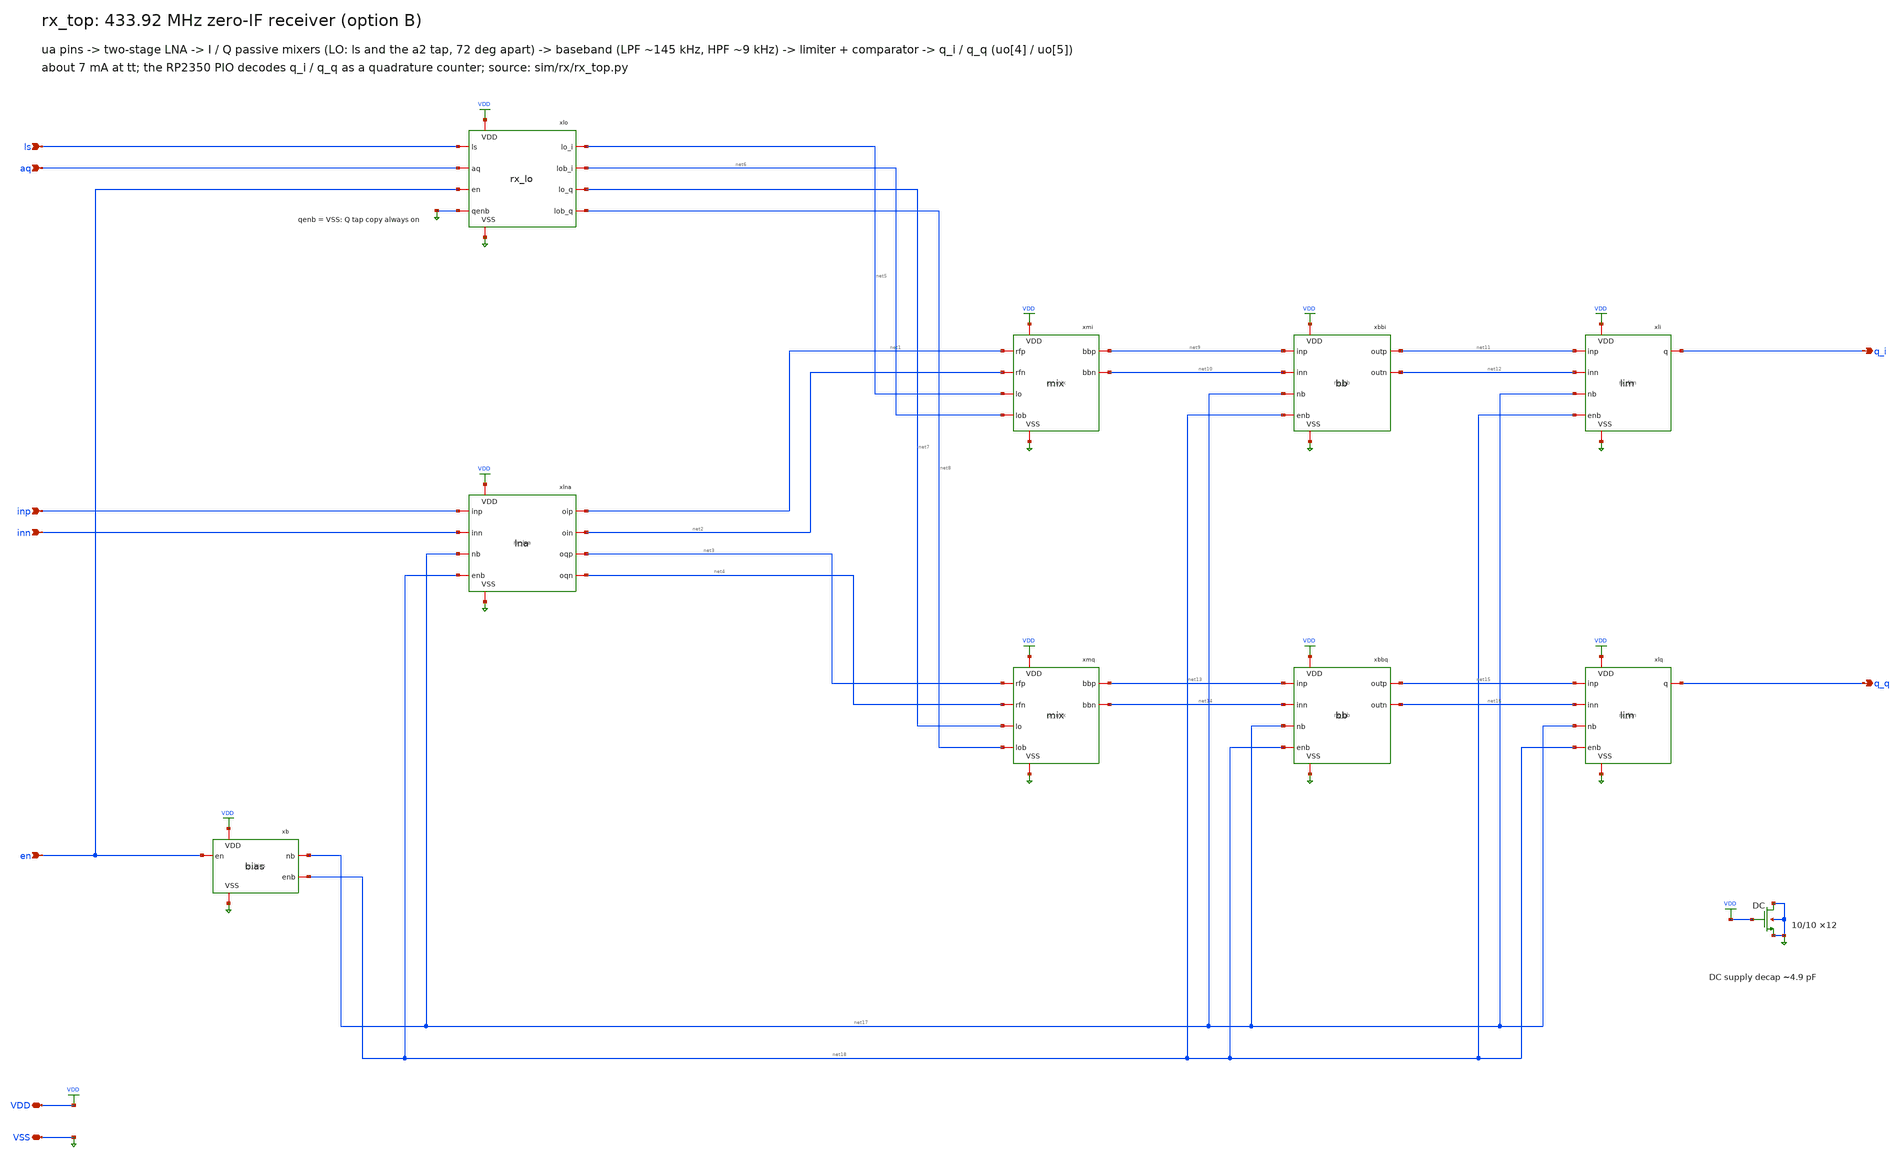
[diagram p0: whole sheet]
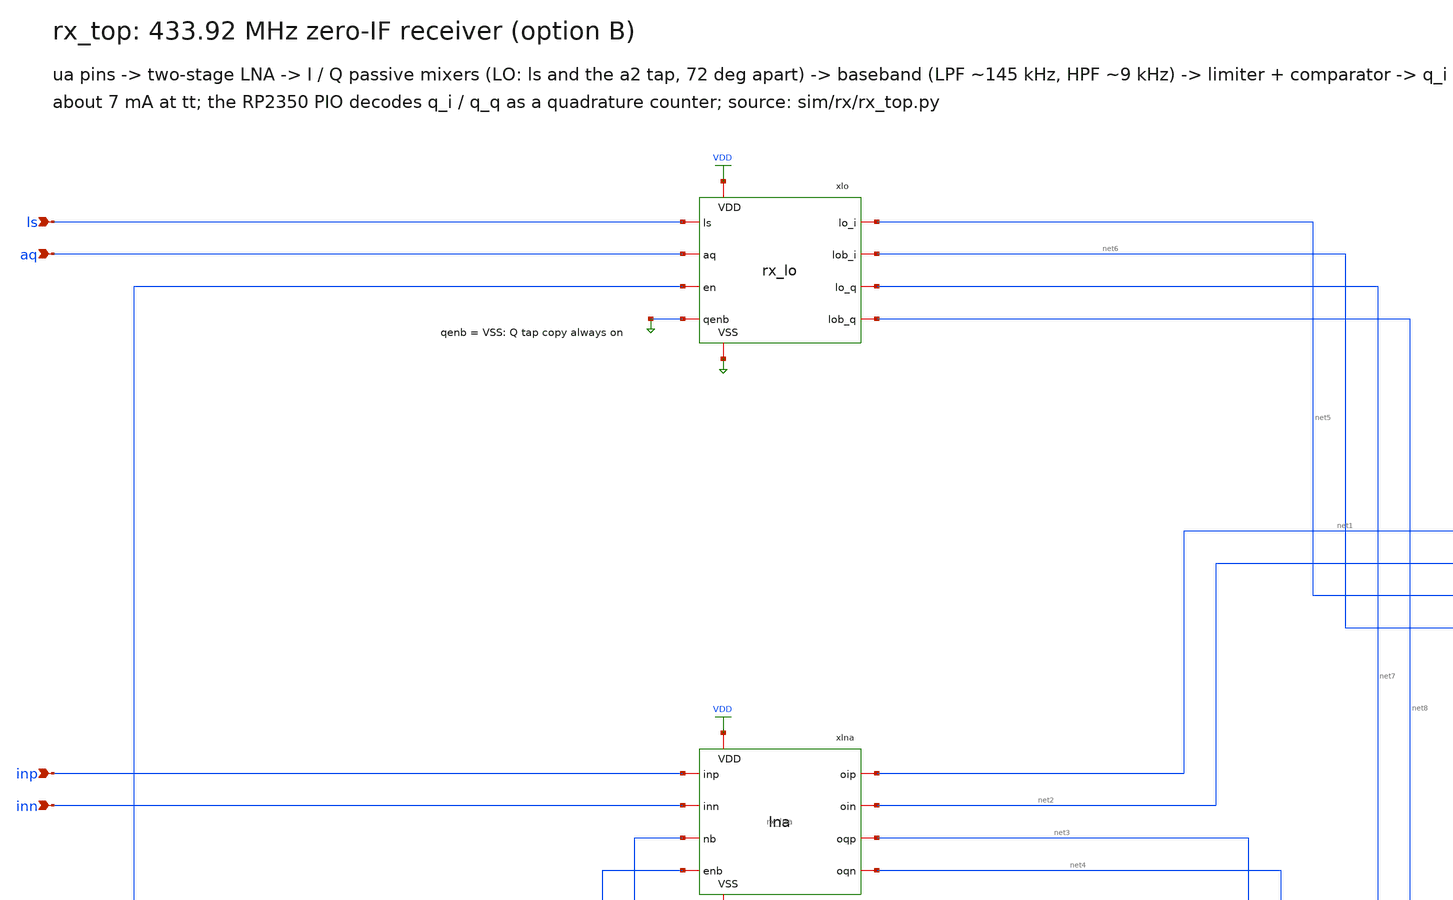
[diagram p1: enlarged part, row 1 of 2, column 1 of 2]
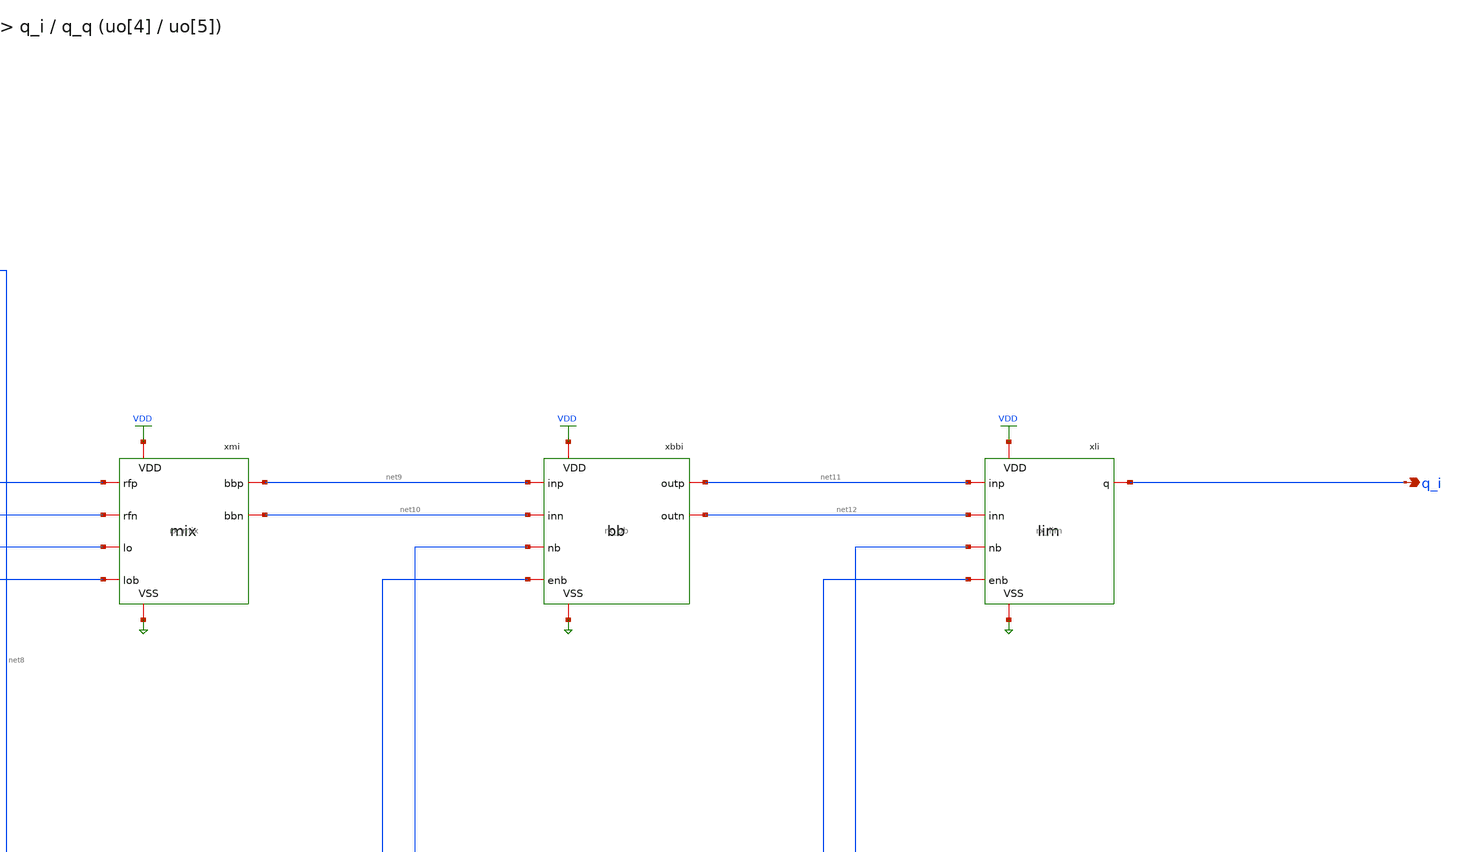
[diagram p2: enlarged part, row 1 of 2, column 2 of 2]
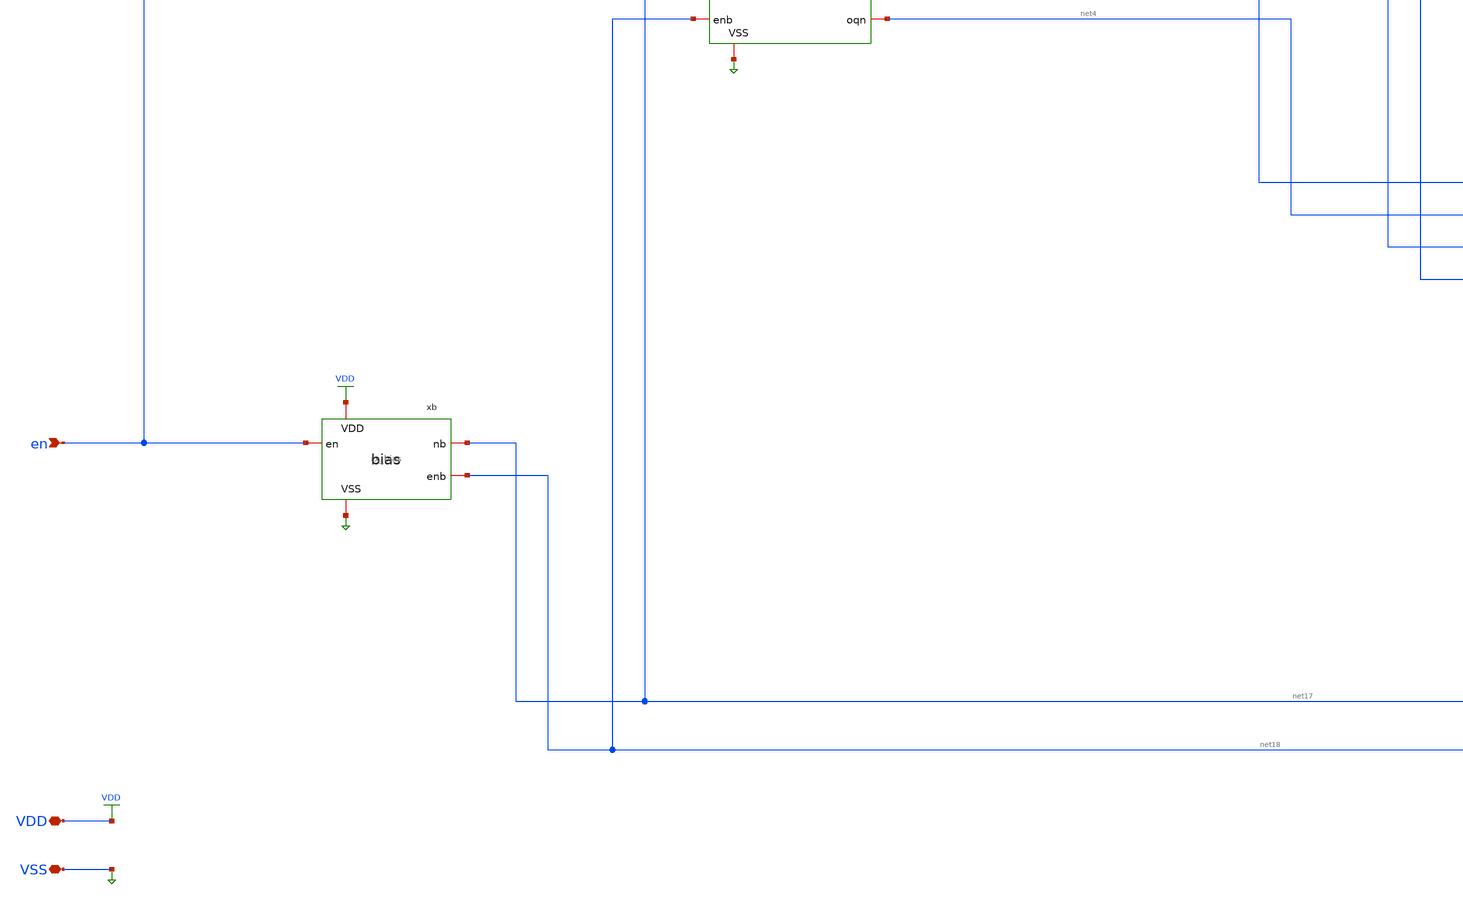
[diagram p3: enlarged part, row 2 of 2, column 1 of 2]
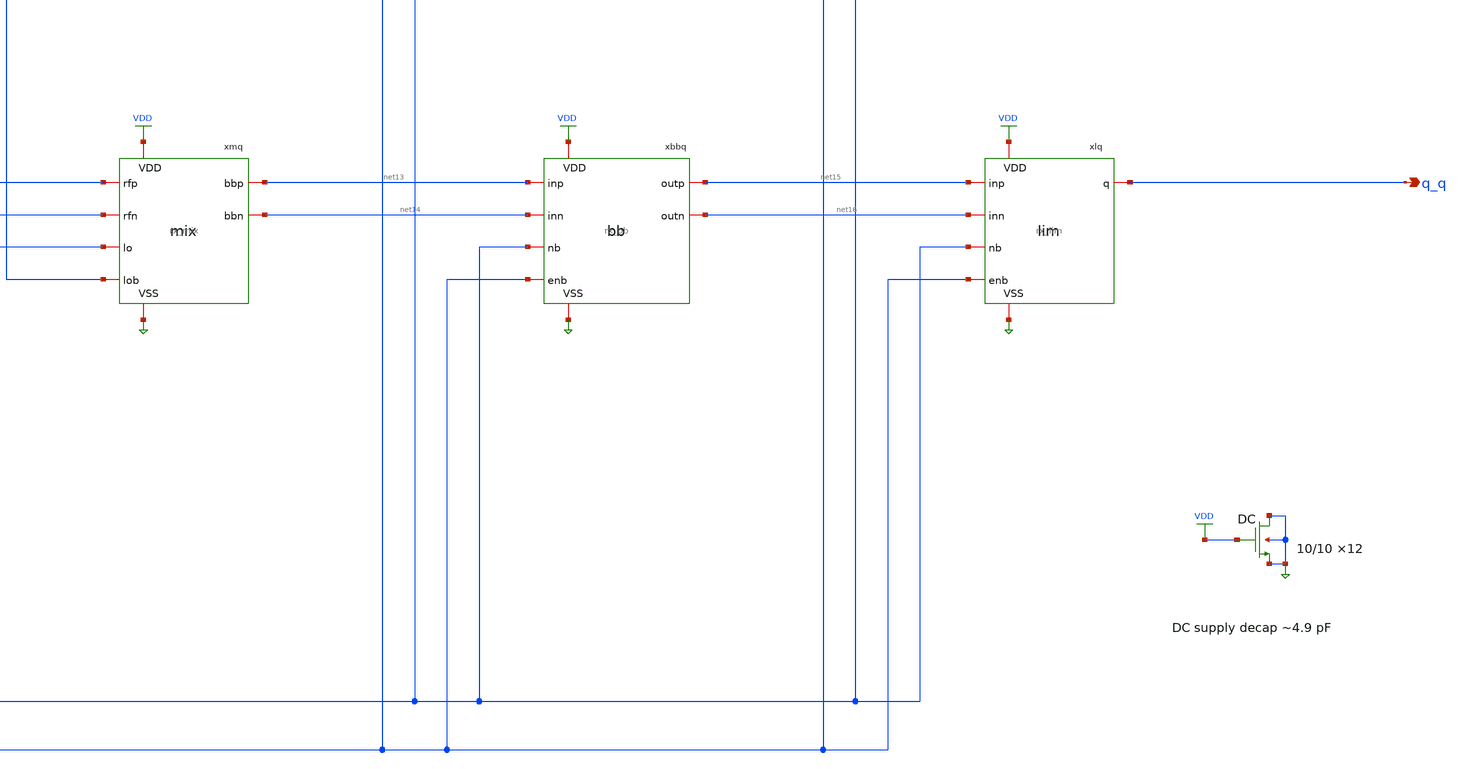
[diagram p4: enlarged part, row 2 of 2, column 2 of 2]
** sch_path: xschem/rx_top.sch
**.subckt rx_top VDD VSS inp inn ls aq en q_i q_q
*.iopin VDD
*.iopin VSS
*.ipin inp
*.ipin inn
*.ipin ls
*.ipin aq
*.ipin en
*.opin q_i
*.opin q_q
xb VDD VSS en net18 net17 rx_bias
xlna VDD VSS inp inn net1 net2 net3 net4 net17 net18 rx_lna
xlo VDD VSS ls aq en VSS net5 net6 net7 net8 rx_lo
xmi VDD VSS net1 net2 net9 net10 net5 net6 rx_mix
xmq VDD VSS net3 net4 net13 net14 net7 net8 rx_mix
xbbi VDD VSS net9 net10 net11 net12 net17 net18 rx_bb
xbbq VDD VSS net13 net14 net15 net16 net17 net18 rx_bb
xli VDD VSS net11 net12 q_i net17 net18 rx_lim
xlq VDD VSS net15 net16 q_q net17 net18 rx_lim
XDC VSS VDD VSS VSS nfet_03v3 L=10.0u W=10.0u nf=1 ad=5.0p as=5.0p pd=21.0u ps=21.0u nrd=0 nrs=0
+ sa=0 sb=0 sd=0 m=12
**.ends

* expanding   symbol:  rx_bias.sym # of pins=5
** sym_path: xschem/rx_bias.sym
** sch_path: xschem/rx_bias.sch
.subckt rx_bias VDD VSS en enb nb
*.iopin VDD
*.iopin VSS
*.ipin en
*.opin enb
*.opin nb
XMsw net2 enb VDD VDD pfet_03v3 L=0.28u W=4.0u nf=1 ad=2.0p as=2.0p pd=9.0u ps=9.0u nrd=0 nrs=0 sa=0
+ sb=0 sd=0 m=1
XMP1 nb net3 net2 VDD pfet_03v3 L=1.0u W=4.0u nf=1 ad=2.0p as=2.0p pd=9.0u ps=9.0u nrd=0 nrs=0 sa=0
+ sb=0 sd=0 m=2
XMP2 net3 net3 net2 VDD pfet_03v3 L=1.0u W=4.0u nf=1 ad=2.0p as=2.0p pd=9.0u ps=9.0u nrd=0 nrs=0
+ sa=0 sb=0 sd=0 m=2
XMN1 nb nb VSS VSS nfet_03v3 L=0.5u W=2.0u nf=1 ad=1.0p as=1.0p pd=5.0u ps=5.0u nrd=0 nrs=0 sa=0
+ sb=0 sd=0 m=1
XMN2 net3 nb net1 VSS nfet_03v3 L=0.5u W=2.0u nf=1 ad=1.0p as=1.0p pd=5.0u ps=5.0u nrd=0 nrs=0 sa=0
+ sb=0 sd=0 m=4
XMS1 net4 VSS net2 VDD pfet_03v3 L=10.0u W=0.41999999999999993u nf=1 ad=0.20999999999999996p
+ as=0.20999999999999996p pd=1.8399999999999999u ps=1.8399999999999999u nrd=0 nrs=0 sa=0 sb=0 sd=0 m=1
XMS2 net4 nb VSS VSS nfet_03v3 L=0.28u W=2.0u nf=1 ad=1.0p as=1.0p pd=5.0u ps=5.0u nrd=0 nrs=0 sa=0
+ sb=0 sd=0 m=1
XMS3 net3 net4 nb VSS nfet_03v3 L=0.28u W=1.0u nf=1 ad=0.5p as=0.5p pd=3.0u ps=3.0u nrd=0 nrs=0 sa=0
+ sb=0 sd=0 m=1
XMoff nb enb VSS VSS nfet_03v3 L=0.28u W=0.41999999999999993u nf=1 ad=0.20999999999999996p
+ as=0.20999999999999996p pd=1.8399999999999999u ps=1.8399999999999999u nrd=0 nrs=0 sa=0 sb=0 sd=0 m=1
XMoff2 net4 enb VSS VSS nfet_03v3 L=0.28u W=0.41999999999999993u nf=1 ad=0.20999999999999996p
+ as=0.20999999999999996p pd=1.8399999999999999u ps=1.8399999999999999u nrd=0 nrs=0 sa=0 sb=0 sd=0 m=1
XRb net1 VSS VSS ppolyf_u r_width=2.0e-6 r_length=29.714000000000002e-6 m=1
XCnb VSS nb VSS VSS nfet_03v3 L=10.0u W=24.57u nf=1 ad=12.285p as=12.285p pd=50.14u ps=50.14u nrd=0
+ nrs=0 sa=0 sb=0 sd=0 m=1
XIep enb en VDD VDD pfet_03v3 L=0.28u W=1.0u nf=1 ad=0.5p as=0.5p pd=3.0u ps=3.0u nrd=0 nrs=0 sa=0
+ sb=0 sd=0 m=1
XIen enb en VSS VSS nfet_03v3 L=0.28u W=0.41999999999999993u nf=1 ad=0.20999999999999996p
+ as=0.20999999999999996p pd=1.8399999999999999u ps=1.8399999999999999u nrd=0 nrs=0 sa=0 sb=0 sd=0 m=1
.ends


* expanding   symbol:  rx_lna.sym # of pins=10
** sym_path: xschem/rx_lna.sym
** sch_path: xschem/rx_lna.sch
.subckt rx_lna VDD VSS inp inn oip oin oqp oqn nb enb
*.iopin VDD
*.iopin VSS
*.ipin inp
*.ipin inn
*.opin oip
*.opin oin
*.opin oqp
*.opin oqn
*.ipin nb
*.ipin enb
XM1 net2 inp net1 VSS nfet_03v3 L=0.28u W=10.0u nf=1 ad=5.0p as=5.0p pd=21.0u ps=21.0u nrd=0 nrs=0
+ sa=0 sb=0 sd=0 m=24
XM2 net3 inn net1 VSS nfet_03v3 L=0.28u W=10.0u nf=1 ad=5.0p as=5.0p pd=21.0u ps=21.0u nrd=0 nrs=0
+ sa=0 sb=0 sd=0 m=24
XMt net1 nb VSS VSS nfet_03v3 L=0.5u W=2.0u nf=1 ad=1.0p as=1.0p pd=5.0u ps=5.0u nrd=0 nrs=0 sa=0
+ sb=0 sd=0 m=120
XRLp net2 VDD VSS ppolyf_u r_width=4.0e-6 r_length=9.143e-6 m=1
XRLn net3 VDD VSS ppolyf_u r_width=4.0e-6 r_length=9.143e-6 m=1
XRgp inp net4 VSS ppolyf_u_1k r_width=1.0e-6 r_length=20.0e-6 m=1
XRgn inn net4 VSS ppolyf_u_1k r_width=1.0e-6 r_length=20.0e-6 m=1
XMvs net5 enb VDD VDD pfet_03v3 L=0.28u W=2.0u nf=1 ad=1.0p as=1.0p pd=5.0u ps=5.0u nrd=0 nrs=0 sa=0
+ sb=0 sd=0 m=1
XRv1 net5 net4 VSS ppolyf_u_1k r_width=1.0e-6 r_length=40.0e-6 m=1
XRv2 net4 VSS VSS ppolyf_u_1k r_width=1.0e-6 r_length=30.0e-6 m=1
XCvcm VSS net4 VSS VSS nfet_03v3 L=10.0u W=49.14u nf=1 ad=24.57p as=24.57p pd=99.28u ps=99.28u nrd=0
+ nrs=0 sa=0 sb=0 sd=0 m=1
x2i VDD VSS net3 net2 oip oin nb rx_lna2
x2q VDD VSS net3 net2 oqp oqn nb rx_lna2
.ends


* expanding   symbol:  rx_lo.sym # of pins=10
** sym_path: xschem/rx_lo.sym
** sch_path: xschem/rx_lo.sch
.subckt rx_lo VDD VSS ls aq en qenb lo_i lob_i lo_q lob_q
*.iopin VDD
*.iopin VSS
*.ipin ls
*.ipin aq
*.ipin en
*.ipin qenb
*.opin lo_i
*.opin lob_i
*.opin lo_q
*.opin lob_q
xlq VDD VSS aq qenb net1 rx_lsq
xbi VDD VSS ls en lo_i lob_i rx_lobuf
xbq VDD VSS net1 en lo_q lob_q rx_lobuf
.ends


* expanding   symbol:  rx_mix.sym # of pins=8
** sym_path: xschem/rx_mix.sym
** sch_path: xschem/rx_mix.sch
.subckt rx_mix VDD VSS rfp rfn bbp bbn lo lob
*.iopin VDD
*.iopin VSS
*.ipin rfp
*.ipin rfn
*.opin bbp
*.opin bbn
*.ipin lo
*.ipin lob
XS1n bbp lo rfp VSS nfet_03v3 L=0.28u W=8.0u nf=1 ad=4.0p as=4.0p pd=17.0u ps=17.0u nrd=0 nrs=0 sa=0
+ sb=0 sd=0 m=1
XS1p bbp lob rfp VDD pfet_03v3 L=0.28u W=16.0u nf=1 ad=8.0p as=8.0p pd=33.0u ps=33.0u nrd=0 nrs=0
+ sa=0 sb=0 sd=0 m=1
XS4n bbn lob rfp VSS nfet_03v3 L=0.28u W=8.0u nf=1 ad=4.0p as=4.0p pd=17.0u ps=17.0u nrd=0 nrs=0
+ sa=0 sb=0 sd=0 m=1
XS4p bbn lo rfp VDD pfet_03v3 L=0.28u W=16.0u nf=1 ad=8.0p as=8.0p pd=33.0u ps=33.0u nrd=0 nrs=0
+ sa=0 sb=0 sd=0 m=1
XS3n bbp lob rfn VSS nfet_03v3 L=0.28u W=8.0u nf=1 ad=4.0p as=4.0p pd=17.0u ps=17.0u nrd=0 nrs=0
+ sa=0 sb=0 sd=0 m=1
XS3p bbp lo rfn VDD pfet_03v3 L=0.28u W=16.0u nf=1 ad=8.0p as=8.0p pd=33.0u ps=33.0u nrd=0 nrs=0
+ sa=0 sb=0 sd=0 m=1
XS2n bbn lo rfn VSS nfet_03v3 L=0.28u W=8.0u nf=1 ad=4.0p as=4.0p pd=17.0u ps=17.0u nrd=0 nrs=0 sa=0
+ sb=0 sd=0 m=1
XS2p bbn lob rfn VDD pfet_03v3 L=0.28u W=16.0u nf=1 ad=8.0p as=8.0p pd=33.0u ps=33.0u nrd=0 nrs=0
+ sa=0 sb=0 sd=0 m=1
XCbp VSS bbp VSS VSS nfet_03v3 L=5.0u W=24.57u nf=1 ad=12.285p as=12.285p pd=50.14u ps=50.14u nrd=0
+ nrs=0 sa=0 sb=0 sd=0 m=1
XCbn VSS bbn VSS VSS nfet_03v3 L=5.0u W=24.57u nf=1 ad=12.285p as=12.285p pd=50.14u ps=50.14u nrd=0
+ nrs=0 sa=0 sb=0 sd=0 m=1
.ends


* expanding   symbol:  rx_bb.sym # of pins=8
** sym_path: xschem/rx_bb.sym
** sch_path: xschem/rx_bb.sch
.subckt rx_bb VDD VSS inp inn outp outn nb enb
*.iopin VDD
*.iopin VSS
*.ipin inp
*.ipin inn
*.opin outp
*.opin outn
*.ipin nb
*.ipin enb
XMvbs net1 enb VDD VDD pfet_03v3 L=0.28u W=1.0u nf=1 ad=0.5p as=0.5p pd=3.0u ps=3.0u nrd=0 nrs=0
+ sa=0 sb=0 sd=0 m=1
XRvb1 net1 net2 VSS ppolyf_u_1k r_width=1.0e-6 r_length=150.0e-6 m=1
XRvb2 net2 VSS VSS ppolyf_u_1k r_width=1.0e-6 r_length=100.0e-6 m=1
XCvb VSS net2 VSS VSS nfet_03v3 L=10.0u W=24.57u nf=1 ad=12.285p as=12.285p pd=50.14u ps=50.14u
+ nrd=0 nrs=0 sa=0 sb=0 sd=0 m=1
XMvbrep net3 net3 net2 net2 pfet_03v3 L=1.0u W=4.0u nf=1 ad=2.0p as=2.0p pd=9.0u ps=9.0u nrd=0 nrs=0
+ sa=0 sb=0 sd=0 m=1
XMvbsnk net3 nb VSS VSS nfet_03v3 L=49.99999999999999u W=0.41999999999999993u nf=1
+ ad=0.20999999999999996p as=0.20999999999999996p pd=1.8399999999999999u ps=1.8399999999999999u nrd=0 nrs=0 sa=0 sb=0 sd=0
+ m=1
XM1a net5 inp net4 VSS nfet_03v3 L=1.0u W=20.0u nf=1 ad=10.0p as=10.0p pd=41.0u ps=41.0u nrd=0 nrs=0
+ sa=0 sb=0 sd=0 m=16
XM1b net6 inn net4 VSS nfet_03v3 L=1.0u W=20.0u nf=1 ad=10.0p as=10.0p pd=41.0u ps=41.0u nrd=0 nrs=0
+ sa=0 sb=0 sd=0 m=16
XMt1 net4 nb VSS VSS nfet_03v3 L=0.5u W=2.0u nf=1 ad=1.0p as=1.0p pd=5.0u ps=5.0u nrd=0 nrs=0 sa=0
+ sb=0 sd=0 m=8
XR1a net5 VDD VSS ppolyf_u r_width=2.0e-6 r_length=57.143e-6 m=1
XR1b net6 VDD VSS ppolyf_u r_width=2.0e-6 r_length=57.143e-6 m=1
XCc2a net6 net7 net6 net6 pfet_03v3 L=10.0u W=24.57u nf=1 ad=12.285p as=12.285p pd=50.14u ps=50.14u
+ nrd=0 nrs=0 sa=0 sb=0 sd=0 m=1
XRp2ar net7 net3 net2 net2 pfet_03v3 L=12.0u W=0.41999999999999993u nf=1 ad=0.20999999999999996p
+ as=0.20999999999999996p pd=1.8399999999999999u ps=1.8399999999999999u nrd=0 nrs=0 sa=0 sb=0 sd=0 m=1
XRp2aa net8 net8 net7 net7 pfet_03v3 L=1.0u W=0.41999999999999993u nf=1 ad=0.20999999999999996p
+ as=0.20999999999999996p pd=1.8399999999999999u ps=1.8399999999999999u nrd=0 nrs=0 sa=0 sb=0 sd=0 m=1
XRp2ab net8 net8 net2 net2 pfet_03v3 L=1.0u W=0.41999999999999993u nf=1 ad=0.20999999999999996p
+ as=0.20999999999999996p pd=1.8399999999999999u ps=1.8399999999999999u nrd=0 nrs=0 sa=0 sb=0 sd=0 m=1
XCc2b net5 net9 net5 net5 pfet_03v3 L=10.0u W=24.57u nf=1 ad=12.285p as=12.285p pd=50.14u ps=50.14u
+ nrd=0 nrs=0 sa=0 sb=0 sd=0 m=1
XRp2br net9 net3 net2 net2 pfet_03v3 L=12.0u W=0.41999999999999993u nf=1 ad=0.20999999999999996p
+ as=0.20999999999999996p pd=1.8399999999999999u ps=1.8399999999999999u nrd=0 nrs=0 sa=0 sb=0 sd=0 m=1
XRp2ba net10 net10 net9 net9 pfet_03v3 L=1.0u W=0.41999999999999993u nf=1 ad=0.20999999999999996p
+ as=0.20999999999999996p pd=1.8399999999999999u ps=1.8399999999999999u nrd=0 nrs=0 sa=0 sb=0 sd=0 m=1
XRp2bb net10 net10 net2 net2 pfet_03v3 L=1.0u W=0.41999999999999993u nf=1 ad=0.20999999999999996p
+ as=0.20999999999999996p pd=1.8399999999999999u ps=1.8399999999999999u nrd=0 nrs=0 sa=0 sb=0 sd=0 m=1
XM2a net12 net7 net11 VSS nfet_03v3 L=1.0u W=4.0u nf=1 ad=2.0p as=2.0p pd=9.0u ps=9.0u nrd=0 nrs=0
+ sa=0 sb=0 sd=0 m=2
XM2b net13 net9 net11 VSS nfet_03v3 L=1.0u W=4.0u nf=1 ad=2.0p as=2.0p pd=9.0u ps=9.0u nrd=0 nrs=0
+ sa=0 sb=0 sd=0 m=2
XMt2f net11 nb VSS VSS nfet_03v3 L=0.5u W=0.3u nf=1 ad=0.15p as=0.15p pd=1.6u ps=1.6u nrd=0 nrs=0
+ sa=0 sb=0 sd=0 m=1
XR2a net12 VDD VSS ppolyf_u_1k r_width=1.0e-6 r_length=200.0e-6 m=1
XR2b net13 VDD VSS ppolyf_u_1k r_width=1.0e-6 r_length=200.0e-6 m=1
XC2a VSS net12 VSS VSS nfet_03v3 L=10.0u W=98.28009999999999u nf=1 ad=49.140049999999995p
+ as=49.140049999999995p pd=197.56019999999998u ps=197.56019999999998u nrd=0 nrs=0 sa=0 sb=0 sd=0 m=1
XC2b VSS net13 VSS VSS nfet_03v3 L=10.0u W=98.28009999999999u nf=1 ad=49.140049999999995p
+ as=49.140049999999995p pd=197.56019999999998u ps=197.56019999999998u nrd=0 nrs=0 sa=0 sb=0 sd=0 m=1
XCc3a net13 net14 net13 net13 pfet_03v3 L=10.0u W=24.57u nf=1 ad=12.285p as=12.285p pd=50.14u
+ ps=50.14u nrd=0 nrs=0 sa=0 sb=0 sd=0 m=1
XRp3ar net14 net3 net2 net2 pfet_03v3 L=12.0u W=0.41999999999999993u nf=1 ad=0.20999999999999996p
+ as=0.20999999999999996p pd=1.8399999999999999u ps=1.8399999999999999u nrd=0 nrs=0 sa=0 sb=0 sd=0 m=1
XRp3aa net15 net15 net14 net14 pfet_03v3 L=1.0u W=0.41999999999999993u nf=1 ad=0.20999999999999996p
+ as=0.20999999999999996p pd=1.8399999999999999u ps=1.8399999999999999u nrd=0 nrs=0 sa=0 sb=0 sd=0 m=1
XRp3ab net15 net15 net2 net2 pfet_03v3 L=1.0u W=0.41999999999999993u nf=1 ad=0.20999999999999996p
+ as=0.20999999999999996p pd=1.8399999999999999u ps=1.8399999999999999u nrd=0 nrs=0 sa=0 sb=0 sd=0 m=1
XCc3b net12 net16 net12 net12 pfet_03v3 L=10.0u W=24.57u nf=1 ad=12.285p as=12.285p pd=50.14u
+ ps=50.14u nrd=0 nrs=0 sa=0 sb=0 sd=0 m=1
XRp3br net16 net3 net2 net2 pfet_03v3 L=12.0u W=0.41999999999999993u nf=1 ad=0.20999999999999996p
+ as=0.20999999999999996p pd=1.8399999999999999u ps=1.8399999999999999u nrd=0 nrs=0 sa=0 sb=0 sd=0 m=1
XRp3ba net17 net17 net16 net16 pfet_03v3 L=1.0u W=0.41999999999999993u nf=1 ad=0.20999999999999996p
+ as=0.20999999999999996p pd=1.8399999999999999u ps=1.8399999999999999u nrd=0 nrs=0 sa=0 sb=0 sd=0 m=1
XRp3bb net17 net17 net2 net2 pfet_03v3 L=1.0u W=0.41999999999999993u nf=1 ad=0.20999999999999996p
+ as=0.20999999999999996p pd=1.8399999999999999u ps=1.8399999999999999u nrd=0 nrs=0 sa=0 sb=0 sd=0 m=1
XM3a outn net14 net18 VSS nfet_03v3 L=1.0u W=4.0u nf=1 ad=2.0p as=2.0p pd=9.0u ps=9.0u nrd=0 nrs=0
+ sa=0 sb=0 sd=0 m=2
XM3b outp net16 net18 VSS nfet_03v3 L=1.0u W=4.0u nf=1 ad=2.0p as=2.0p pd=9.0u ps=9.0u nrd=0 nrs=0
+ sa=0 sb=0 sd=0 m=2
XMt3f net18 nb VSS VSS nfet_03v3 L=0.5u W=0.7999999999999999u nf=1 ad=0.39999999999999997p
+ as=0.39999999999999997p pd=2.5999999999999996u ps=2.5999999999999996u nrd=0 nrs=0 sa=0 sb=0 sd=0 m=1
XR3a outn VDD VSS ppolyf_u_1k r_width=1.0e-6 r_length=200.0e-6 m=1
XR3b outp VDD VSS ppolyf_u_1k r_width=1.0e-6 r_length=200.0e-6 m=1
XC3a VSS outn VSS VSS nfet_03v3 L=10.0u W=98.28009999999999u nf=1 ad=49.140049999999995p
+ as=49.140049999999995p pd=197.56019999999998u ps=197.56019999999998u nrd=0 nrs=0 sa=0 sb=0 sd=0 m=1
XC3b VSS outp VSS VSS nfet_03v3 L=10.0u W=98.28009999999999u nf=1 ad=49.140049999999995p
+ as=49.140049999999995p pd=197.56019999999998u ps=197.56019999999998u nrd=0 nrs=0 sa=0 sb=0 sd=0 m=1
.ends


* expanding   symbol:  rx_lim.sym # of pins=7
** sym_path: xschem/rx_lim.sym
** sch_path: xschem/rx_lim.sch
.subckt rx_lim VDD VSS inp inn q nb enb
*.iopin VDD
*.iopin VSS
*.ipin inp
*.ipin inn
*.opin q
*.ipin nb
*.ipin enb
XMvbs net1 enb VDD VDD pfet_03v3 L=0.28u W=1.0u nf=1 ad=0.5p as=0.5p pd=3.0u ps=3.0u nrd=0 nrs=0
+ sa=0 sb=0 sd=0 m=1
XRvb1 net1 net2 VSS ppolyf_u_1k r_width=1.0e-6 r_length=150.0e-6 m=1
XRvb2 net2 VSS VSS ppolyf_u_1k r_width=1.0e-6 r_length=100.0e-6 m=1
XCvb VSS net2 VSS VSS nfet_03v3 L=10.0u W=24.57u nf=1 ad=12.285p as=12.285p pd=50.14u ps=50.14u
+ nrd=0 nrs=0 sa=0 sb=0 sd=0 m=1
XMvbrep net3 net3 net2 net2 pfet_03v3 L=1.0u W=4.0u nf=1 ad=2.0p as=2.0p pd=9.0u ps=9.0u nrd=0 nrs=0
+ sa=0 sb=0 sd=0 m=1
XMvbsnk net3 nb VSS VSS nfet_03v3 L=49.99999999999999u W=0.41999999999999993u nf=1
+ ad=0.20999999999999996p as=0.20999999999999996p pd=1.8399999999999999u ps=1.8399999999999999u nrd=0 nrs=0 sa=0 sb=0 sd=0
+ m=1
XCcLa inp net4 inp inp pfet_03v3 L=10.0u W=12.285u nf=1 ad=6.1425p as=6.1425p pd=25.57u ps=25.57u
+ nrd=0 nrs=0 sa=0 sb=0 sd=0 m=1
XRpLar net4 net3 net2 net2 pfet_03v3 L=12.0u W=0.41999999999999993u nf=1 ad=0.20999999999999996p
+ as=0.20999999999999996p pd=1.8399999999999999u ps=1.8399999999999999u nrd=0 nrs=0 sa=0 sb=0 sd=0 m=1
XRpLaa net5 net5 net4 net4 pfet_03v3 L=1.0u W=0.41999999999999993u nf=1 ad=0.20999999999999996p
+ as=0.20999999999999996p pd=1.8399999999999999u ps=1.8399999999999999u nrd=0 nrs=0 sa=0 sb=0 sd=0 m=1
XRpLab net5 net5 net2 net2 pfet_03v3 L=1.0u W=0.41999999999999993u nf=1 ad=0.20999999999999996p
+ as=0.20999999999999996p pd=1.8399999999999999u ps=1.8399999999999999u nrd=0 nrs=0 sa=0 sb=0 sd=0 m=1
XCcLb inn net6 inn inn pfet_03v3 L=10.0u W=12.285u nf=1 ad=6.1425p as=6.1425p pd=25.57u ps=25.57u
+ nrd=0 nrs=0 sa=0 sb=0 sd=0 m=1
XRpLbr net6 net3 net2 net2 pfet_03v3 L=12.0u W=0.41999999999999993u nf=1 ad=0.20999999999999996p
+ as=0.20999999999999996p pd=1.8399999999999999u ps=1.8399999999999999u nrd=0 nrs=0 sa=0 sb=0 sd=0 m=1
XRpLba net7 net7 net6 net6 pfet_03v3 L=1.0u W=0.41999999999999993u nf=1 ad=0.20999999999999996p
+ as=0.20999999999999996p pd=1.8399999999999999u ps=1.8399999999999999u nrd=0 nrs=0 sa=0 sb=0 sd=0 m=1
XRpLbb net7 net7 net2 net2 pfet_03v3 L=1.0u W=0.41999999999999993u nf=1 ad=0.20999999999999996p
+ as=0.20999999999999996p pd=1.8399999999999999u ps=1.8399999999999999u nrd=0 nrs=0 sa=0 sb=0 sd=0 m=1
XMLa net9 net4 net8 VSS nfet_03v3 L=0.5u W=4.0u nf=1 ad=2.0p as=2.0p pd=9.0u ps=9.0u nrd=0 nrs=0
+ sa=0 sb=0 sd=0 m=2
XMLb net10 net6 net8 VSS nfet_03v3 L=0.5u W=4.0u nf=1 ad=2.0p as=2.0p pd=9.0u ps=9.0u nrd=0 nrs=0
+ sa=0 sb=0 sd=0 m=2
XMtL net8 nb VSS VSS nfet_03v3 L=0.5u W=2.0u nf=1 ad=1.0p as=1.0p pd=5.0u ps=5.0u nrd=0 nrs=0 sa=0
+ sb=0 sd=0 m=1
XRLa net9 VDD VSS ppolyf_u r_width=1.0e-6 r_length=28.571e-6 m=1
XRLb net10 VDD VSS ppolyf_u r_width=1.0e-6 r_length=28.571e-6 m=1
XCcCa net10 net11 net10 net10 pfet_03v3 L=10.0u W=12.285u nf=1 ad=6.1425p as=6.1425p pd=25.57u
+ ps=25.57u nrd=0 nrs=0 sa=0 sb=0 sd=0 m=1
XRpCar net11 net3 net2 net2 pfet_03v3 L=12.0u W=0.41999999999999993u nf=1 ad=0.20999999999999996p
+ as=0.20999999999999996p pd=1.8399999999999999u ps=1.8399999999999999u nrd=0 nrs=0 sa=0 sb=0 sd=0 m=1
XRpCaa net12 net12 net11 net11 pfet_03v3 L=1.0u W=0.41999999999999993u nf=1 ad=0.20999999999999996p
+ as=0.20999999999999996p pd=1.8399999999999999u ps=1.8399999999999999u nrd=0 nrs=0 sa=0 sb=0 sd=0 m=1
XRpCab net12 net12 net2 net2 pfet_03v3 L=1.0u W=0.41999999999999993u nf=1 ad=0.20999999999999996p
+ as=0.20999999999999996p pd=1.8399999999999999u ps=1.8399999999999999u nrd=0 nrs=0 sa=0 sb=0 sd=0 m=1
XCcCb net9 net13 net9 net9 pfet_03v3 L=10.0u W=12.285u nf=1 ad=6.1425p as=6.1425p pd=25.57u
+ ps=25.57u nrd=0 nrs=0 sa=0 sb=0 sd=0 m=1
XRpCbr net13 net3 net2 net2 pfet_03v3 L=12.0u W=0.41999999999999993u nf=1 ad=0.20999999999999996p
+ as=0.20999999999999996p pd=1.8399999999999999u ps=1.8399999999999999u nrd=0 nrs=0 sa=0 sb=0 sd=0 m=1
XRpCba net14 net14 net13 net13 pfet_03v3 L=1.0u W=0.41999999999999993u nf=1 ad=0.20999999999999996p
+ as=0.20999999999999996p pd=1.8399999999999999u ps=1.8399999999999999u nrd=0 nrs=0 sa=0 sb=0 sd=0 m=1
XRpCbb net14 net14 net2 net2 pfet_03v3 L=1.0u W=0.41999999999999993u nf=1 ad=0.20999999999999996p
+ as=0.20999999999999996p pd=1.8399999999999999u ps=1.8399999999999999u nrd=0 nrs=0 sa=0 sb=0 sd=0 m=1
XC1 net16 net11 net15 VSS nfet_03v3 L=0.5u W=2.0u nf=1 ad=1.0p as=1.0p pd=5.0u ps=5.0u nrd=0 nrs=0
+ sa=0 sb=0 sd=0 m=2
XC2 net17 net13 net15 VSS nfet_03v3 L=0.5u W=2.0u nf=1 ad=1.0p as=1.0p pd=5.0u ps=5.0u nrd=0 nrs=0
+ sa=0 sb=0 sd=0 m=2
XCt net15 nb VSS VSS nfet_03v3 L=0.5u W=2.0u nf=1 ad=1.0p as=1.0p pd=5.0u ps=5.0u nrd=0 nrs=0 sa=0
+ sb=0 sd=0 m=1
XC3 net16 net16 VDD VDD pfet_03v3 L=0.5u W=1.0u nf=1 ad=0.5p as=0.5p pd=3.0u ps=3.0u nrd=0 nrs=0
+ sa=0 sb=0 sd=0 m=1
XC5 net16 net17 VDD VDD pfet_03v3 L=0.5u W=1.6999999999999997u nf=1 ad=0.8499999999999999p
+ as=0.8499999999999999p pd=4.3999999999999995u ps=4.3999999999999995u nrd=0 nrs=0 sa=0 sb=0 sd=0 m=1
XC4 net17 net17 VDD VDD pfet_03v3 L=0.5u W=1.0u nf=1 ad=0.5p as=0.5p pd=3.0u ps=3.0u nrd=0 nrs=0
+ sa=0 sb=0 sd=0 m=1
XC6 net17 net16 VDD VDD pfet_03v3 L=0.5u W=1.6999999999999997u nf=1 ad=0.8499999999999999p
+ as=0.8499999999999999p pd=4.3999999999999995u ps=4.3999999999999995u nrd=0 nrs=0 sa=0 sb=0 sd=0 m=1
XC7 net18 net17 VDD VDD pfet_03v3 L=0.5u W=2.0u nf=1 ad=1.0p as=1.0p pd=5.0u ps=5.0u nrd=0 nrs=0
+ sa=0 sb=0 sd=0 m=1
XC8 net19 net16 VDD VDD pfet_03v3 L=0.5u W=2.0u nf=1 ad=1.0p as=1.0p pd=5.0u ps=5.0u nrd=0 nrs=0
+ sa=0 sb=0 sd=0 m=1
XC9 net18 net18 VSS VSS nfet_03v3 L=0.5u W=1.0u nf=1 ad=0.5p as=0.5p pd=3.0u ps=3.0u nrd=0 nrs=0
+ sa=0 sb=0 sd=0 m=1
XC10 net19 net18 VSS VSS nfet_03v3 L=0.5u W=1.0u nf=1 ad=0.5p as=0.5p pd=3.0u ps=3.0u nrd=0 nrs=0
+ sa=0 sb=0 sd=0 m=1
XB1p net20 net19 VDD VDD pfet_03v3 L=0.28u W=1.25u nf=1 ad=0.625p as=0.625p pd=3.5u ps=3.5u nrd=0
+ nrs=0 sa=0 sb=0 sd=0 m=1
XB1n net20 net19 VSS VSS nfet_03v3 L=0.28u W=0.5u nf=1 ad=0.25p as=0.25p pd=2.0u ps=2.0u nrd=0 nrs=0
+ sa=0 sb=0 sd=0 m=1
XB2p q net20 VDD VDD pfet_03v3 L=0.28u W=5.0u nf=1 ad=2.5p as=2.5p pd=11.0u ps=11.0u nrd=0 nrs=0
+ sa=0 sb=0 sd=0 m=1
XB2n q net20 VSS VSS nfet_03v3 L=0.28u W=2.0u nf=1 ad=1.0p as=1.0p pd=5.0u ps=5.0u nrd=0 nrs=0 sa=0
+ sb=0 sd=0 m=1
.ends


* expanding   symbol:  rx_lna2.sym # of pins=7
** sym_path: xschem/rx_lna2.sym
** sch_path: xschem/rx_lna2.sch
.subckt rx_lna2 VDD VSS ip im op om nb
*.iopin VDD
*.iopin VSS
*.ipin ip
*.ipin im
*.opin op
*.opin om
*.ipin nb
XM1 om ip net1 VSS nfet_03v3 L=0.28u W=10.0u nf=1 ad=5.0p as=5.0p pd=21.0u ps=21.0u nrd=0 nrs=0 sa=0
+ sb=0 sd=0 m=6
XM2 op im net1 VSS nfet_03v3 L=0.28u W=10.0u nf=1 ad=5.0p as=5.0p pd=21.0u ps=21.0u nrd=0 nrs=0 sa=0
+ sb=0 sd=0 m=6
XMt net1 nb VSS VSS nfet_03v3 L=0.5u W=2.0u nf=1 ad=1.0p as=1.0p pd=5.0u ps=5.0u nrd=0 nrs=0 sa=0
+ sb=0 sd=0 m=40
XRLp om VDD VSS ppolyf_u r_width=2.0e-6 r_length=9.143e-6 m=1
XRLn op VDD VSS ppolyf_u r_width=2.0e-6 r_length=9.143e-6 m=1
.ends


* expanding   symbol:  rx_lsq.sym # of pins=5
** sym_path: xschem/rx_lsq.sym
** sch_path: xschem/rx_lsq.sch
.subckt rx_lsq VDD VSS aq qenb lsq
*.iopin VDD
*.iopin VSS
*.ipin aq
*.ipin qenb
*.opin lsq
XHq net2 qenb VDD VDD pfet_03v3 L=0.28u W=10.0u nf=1 ad=5.0p as=5.0p pd=21.0u ps=21.0u nrd=0 nrs=0
+ sa=0 sb=0 sd=0 m=2
XCq VSS net2 VSS VSS nfet_03v3 L=10.0u W=24.57u nf=1 ad=12.285p as=12.285p pd=50.14u ps=50.14u nrd=0
+ nrs=0 sa=0 sb=0 sd=0 m=1
xls net2 VSS aq lsq ls_ac
xd1 net2 VSS lsq net3 tspc_t1
XTTp net1 lsq net2 net2 pfet_03v3 L=0.28u W=1.0499999999999998u nf=1 ad=0.5249999999999999p
+ as=0.5249999999999999p pd=3.0999999999999996u ps=3.0999999999999996u nrd=0 nrs=0 sa=0 sb=0 sd=0 m=1
XTTn net1 lsq VSS VSS nfet_03v3 L=0.28u W=0.41999999999999993u nf=1 ad=0.20999999999999996p
+ as=0.20999999999999996p pd=1.8399999999999999u ps=1.8399999999999999u nrd=0 nrs=0 sa=0 sb=0 sd=0 m=1
XDq lsq qenb VSS VSS nfet_03v3 L=0.28u W=0.41999999999999993u nf=1 ad=0.20999999999999996p
+ as=0.20999999999999996p pd=1.8399999999999999u ps=1.8399999999999999u nrd=0 nrs=0 sa=0 sb=0 sd=0 m=1
.ends


* expanding   symbol:  rx_lobuf.sym # of pins=6
** sym_path: xschem/rx_lobuf.sym
** sch_path: xschem/rx_lobuf.sch
.subckt rx_lobuf VDD VSS in en lo lob
*.iopin VDD
*.iopin VSS
*.ipin in
*.ipin en
*.opin lo
*.opin lob
XG0a net1 in VDD VDD pfet_03v3 L=0.28u W=0.6u nf=1 ad=0.3p as=0.3p pd=2.2u ps=2.2u nrd=0 nrs=0 sa=0
+ sb=0 sd=0 m=1
XG0b net1 en VDD VDD pfet_03v3 L=0.28u W=0.6u nf=1 ad=0.3p as=0.3p pd=2.2u ps=2.2u nrd=0 nrs=0 sa=0
+ sb=0 sd=0 m=1
XG0c net1 in net2 VSS nfet_03v3 L=0.28u W=0.5u nf=1 ad=0.25p as=0.25p pd=2.0u ps=2.0u nrd=0 nrs=0
+ sa=0 sb=0 sd=0 m=1
XG0d net2 en VSS VSS nfet_03v3 L=0.28u W=0.5u nf=1 ad=0.25p as=0.25p pd=2.0u ps=2.0u nrd=0 nrs=0
+ sa=0 sb=0 sd=0 m=1
XTp net3 net1 VDD VDD pfet_03v3 L=0.28u W=1.0499999999999998u nf=1 ad=0.5249999999999999p
+ as=0.5249999999999999p pd=3.0999999999999996u ps=3.0999999999999996u nrd=0 nrs=0 sa=0 sb=0 sd=0 m=1
XTn net3 net1 VSS VSS nfet_03v3 L=0.28u W=0.41999999999999993u nf=1 ad=0.20999999999999996p
+ as=0.20999999999999996p pd=1.8399999999999999u ps=1.8399999999999999u nrd=0 nrs=0 sa=0 sb=0 sd=0 m=1
XA1p net4 net3 VDD VDD pfet_03v3 L=0.28u W=1.25u nf=1 ad=0.625p as=0.625p pd=3.5u ps=3.5u nrd=0
+ nrs=0 sa=0 sb=0 sd=0 m=1
XA1n net4 net3 VSS VSS nfet_03v3 L=0.28u W=0.5u nf=1 ad=0.25p as=0.25p pd=2.0u ps=2.0u nrd=0 nrs=0
+ sa=0 sb=0 sd=0 m=1
XA2p net5 net4 VDD VDD pfet_03v3 L=0.28u W=2.5u nf=1 ad=1.25p as=1.25p pd=6.0u ps=6.0u nrd=0 nrs=0
+ sa=0 sb=0 sd=0 m=1
XA2n net5 net4 VSS VSS nfet_03v3 L=0.28u W=1.0u nf=1 ad=0.5p as=0.5p pd=3.0u ps=3.0u nrd=0 nrs=0
+ sa=0 sb=0 sd=0 m=1
XB1p net6 net3 VDD VDD pfet_03v3 L=0.28u W=3.7499999999999996u nf=1 ad=1.8749999999999998p
+ as=1.8749999999999998p pd=8.5u ps=8.5u nrd=0 nrs=0 sa=0 sb=0 sd=0 m=1
XB1n net6 net3 VSS VSS nfet_03v3 L=0.28u W=1.5u nf=1 ad=0.75p as=0.75p pd=4.0u ps=4.0u nrd=0 nrs=0
+ sa=0 sb=0 sd=0 m=1
XTGp net7 VSS net6 VDD pfet_03v3 L=0.28u W=2.5u nf=1 ad=1.25p as=1.25p pd=6.0u ps=6.0u nrd=0 nrs=0
+ sa=0 sb=0 sd=0 m=1
XTGn net7 VDD net6 VSS nfet_03v3 L=0.28u W=1.0u nf=1 ad=0.5p as=0.5p pd=3.0u ps=3.0u nrd=0 nrs=0
+ sa=0 sb=0 sd=0 m=1
XXBp net7 net5 VDD VDD pfet_03v3 L=0.28u W=1.0499999999999998u nf=1 ad=0.5249999999999999p
+ as=0.5249999999999999p pd=3.0999999999999996u ps=3.0999999999999996u nrd=0 nrs=0 sa=0 sb=0 sd=0 m=1
XXBn net7 net5 VSS VSS nfet_03v3 L=0.28u W=0.41999999999999993u nf=1 ad=0.20999999999999996p
+ as=0.20999999999999996p pd=1.8399999999999999u ps=1.8399999999999999u nrd=0 nrs=0 sa=0 sb=0 sd=0 m=1
XXAp net5 net7 VDD VDD pfet_03v3 L=0.28u W=1.0499999999999998u nf=1 ad=0.5249999999999999p
+ as=0.5249999999999999p pd=3.0999999999999996u ps=3.0999999999999996u nrd=0 nrs=0 sa=0 sb=0 sd=0 m=1
XXAn net5 net7 VSS VSS nfet_03v3 L=0.28u W=0.41999999999999993u nf=1 ad=0.20999999999999996p
+ as=0.20999999999999996p pd=1.8399999999999999u ps=1.8399999999999999u nrd=0 nrs=0 sa=0 sb=0 sd=0 m=1
XPGa net8 net5 VDD VDD pfet_03v3 L=0.28u W=1.25u nf=1 ad=0.625p as=0.625p pd=3.5u ps=3.5u nrd=0
+ nrs=0 sa=0 sb=0 sd=0 m=1
XPGb net8 en VDD VDD pfet_03v3 L=0.28u W=1.25u nf=1 ad=0.625p as=0.625p pd=3.5u ps=3.5u nrd=0 nrs=0
+ sa=0 sb=0 sd=0 m=1
XPGc net8 net5 net9 VSS nfet_03v3 L=0.28u W=1.0u nf=1 ad=0.5p as=0.5p pd=3.0u ps=3.0u nrd=0 nrs=0
+ sa=0 sb=0 sd=0 m=1
XPGd net9 en VSS VSS nfet_03v3 L=0.28u W=1.0u nf=1 ad=0.5p as=0.5p pd=3.0u ps=3.0u nrd=0 nrs=0 sa=0
+ sb=0 sd=0 m=1
XP1p net10 net8 VDD VDD pfet_03v3 L=0.28u W=2.0u nf=1 ad=1.0p as=1.0p pd=5.0u ps=5.0u nrd=0 nrs=0
+ sa=0 sb=0 sd=0 m=1
XP1n net10 net8 VSS VSS nfet_03v3 L=0.28u W=0.7999999999999999u nf=1 ad=0.39999999999999997p
+ as=0.39999999999999997p pd=2.5999999999999996u ps=2.5999999999999996u nrd=0 nrs=0 sa=0 sb=0 sd=0 m=1
XP2p net11 net10 VDD VDD pfet_03v3 L=0.28u W=5.0u nf=1 ad=2.5p as=2.5p pd=11.0u ps=11.0u nrd=0 nrs=0
+ sa=0 sb=0 sd=0 m=1
XP2n net11 net10 VSS VSS nfet_03v3 L=0.28u W=2.0u nf=1 ad=1.0p as=1.0p pd=5.0u ps=5.0u nrd=0 nrs=0
+ sa=0 sb=0 sd=0 m=1
XP3p lo net11 VDD VDD pfet_03v3 L=0.28u W=12.499999999999998u nf=1 ad=6.249999999999999p
+ as=6.249999999999999p pd=25.999999999999996u ps=25.999999999999996u nrd=0 nrs=0 sa=0 sb=0 sd=0 m=1
XP3n lo net11 VSS VSS nfet_03v3 L=0.28u W=5.0u nf=1 ad=2.5p as=2.5p pd=11.0u ps=11.0u nrd=0 nrs=0
+ sa=0 sb=0 sd=0 m=1
XNGa net12 net7 VDD VDD pfet_03v3 L=0.28u W=1.25u nf=1 ad=0.625p as=0.625p pd=3.5u ps=3.5u nrd=0
+ nrs=0 sa=0 sb=0 sd=0 m=1
XNGb net12 en VDD VDD pfet_03v3 L=0.28u W=1.25u nf=1 ad=0.625p as=0.625p pd=3.5u ps=3.5u nrd=0 nrs=0
+ sa=0 sb=0 sd=0 m=1
XNGc net12 net7 net13 VSS nfet_03v3 L=0.28u W=1.0u nf=1 ad=0.5p as=0.5p pd=3.0u ps=3.0u nrd=0 nrs=0
+ sa=0 sb=0 sd=0 m=1
XNGd net13 en VSS VSS nfet_03v3 L=0.28u W=1.0u nf=1 ad=0.5p as=0.5p pd=3.0u ps=3.0u nrd=0 nrs=0 sa=0
+ sb=0 sd=0 m=1
XN1p net14 net12 VDD VDD pfet_03v3 L=0.28u W=2.0u nf=1 ad=1.0p as=1.0p pd=5.0u ps=5.0u nrd=0 nrs=0
+ sa=0 sb=0 sd=0 m=1
XN1n net14 net12 VSS VSS nfet_03v3 L=0.28u W=0.7999999999999999u nf=1 ad=0.39999999999999997p
+ as=0.39999999999999997p pd=2.5999999999999996u ps=2.5999999999999996u nrd=0 nrs=0 sa=0 sb=0 sd=0 m=1
XN2p net15 net14 VDD VDD pfet_03v3 L=0.28u W=5.0u nf=1 ad=2.5p as=2.5p pd=11.0u ps=11.0u nrd=0 nrs=0
+ sa=0 sb=0 sd=0 m=1
XN2n net15 net14 VSS VSS nfet_03v3 L=0.28u W=2.0u nf=1 ad=1.0p as=1.0p pd=5.0u ps=5.0u nrd=0 nrs=0
+ sa=0 sb=0 sd=0 m=1
XN3p lob net15 VDD VDD pfet_03v3 L=0.28u W=12.499999999999998u nf=1 ad=6.249999999999999p
+ as=6.249999999999999p pd=25.999999999999996u ps=25.999999999999996u nrd=0 nrs=0 sa=0 sb=0 sd=0 m=1
XN3n lob net15 VSS VSS nfet_03v3 L=0.28u W=5.0u nf=1 ad=2.5p as=2.5p pd=11.0u ps=11.0u nrd=0 nrs=0
+ sa=0 sb=0 sd=0 m=1
.ends


* expanding   symbol:  ls_ac.sym # of pins=4
** sym_path: xschem/ls_ac.sym
** sch_path: xschem/ls_ac.sch
.subckt ls_ac VDD VSS a0 ls
*.iopin VDD
*.iopin VSS
*.ipin a0
*.opin ls
XL1p net2 net1 VDD VDD pfet_03v3 L=0.28u W=0.5u nf=1 ad=0.25p as=0.25p pd=2.0u ps=2.0u nrd=0 nrs=0
+ sa=0 sb=0 sd=0 m=1
XL1n net2 net1 VSS VSS nfet_03v3 L=0.28u W=0.21999999999999997u nf=1 ad=0.10999999999999999p
+ as=0.10999999999999999p pd=1.44u ps=1.44u nrd=0 nrs=0 sa=0 sb=0 sd=0 m=1
XL2p net3 net2 VDD VDD pfet_03v3 L=0.28u W=1.5u nf=1 ad=0.75p as=0.75p pd=4.0u ps=4.0u nrd=0 nrs=0
+ sa=0 sb=0 sd=0 m=1
XL2n net3 net2 VSS VSS nfet_03v3 L=0.28u W=0.6u nf=1 ad=0.3p as=0.3p pd=2.2u ps=2.2u nrd=0 nrs=0
+ sa=0 sb=0 sd=0 m=1
XL3p ls net3 VDD VDD pfet_03v3 L=0.28u W=3.0u nf=1 ad=1.5p as=1.5p pd=7.0u ps=7.0u nrd=0 nrs=0 sa=0
+ sb=0 sd=0 m=1
XL3n ls net3 VSS VSS nfet_03v3 L=0.28u W=1.2u nf=1 ad=0.6p as=0.6p pd=3.4u ps=3.4u nrd=0 nrs=0 sa=0
+ sb=0 sd=0 m=1
Cc a0 net1 2e-15 m=1
XLRB net1 VSS net4 VDD pfet_03v3 L=2.0u W=0.21999999999999997u nf=1 ad=0.10999999999999999p
+ as=0.10999999999999999p pd=1.44u ps=1.44u nrd=0 nrs=0 sa=0 sb=0 sd=0 m=1
XR1 ls net4 VSS ppolyf_u_1k r_width=1.0e-6 r_length=159.125e-6 m=1
XC1 VSS net4 VSS VSS nfet_03v3 L=16.0u W=16.0u nf=1 ad=8.0p as=8.0p pd=33.0u ps=33.0u nrd=0 nrs=0
+ sa=0 sb=0 sd=0 m=1
.ends


* expanding   symbol:  tspc_t1.sym # of pins=4
** sym_path: xschem/tspc_t1.sym
** sch_path: xschem/tspc_t1.sch
.subckt tspc_t1 VDD VSS clk q
*.iopin VDD
*.iopin VSS
*.ipin clk
*.opin q
Xp1 net1 net6 VDD VDD pfet_03v3 L=0.28u W=2.0u nf=1 ad=1.0p as=1.0p pd=5.0u ps=5.0u nrd=0 nrs=0 sa=0
+ sb=0 sd=0 m=1
Xp2 net4 clk net1 VDD pfet_03v3 L=0.28u W=2.0u nf=1 ad=1.0p as=1.0p pd=5.0u ps=5.0u nrd=0 nrs=0 sa=0
+ sb=0 sd=0 m=1
Xn1 net4 net6 VSS VSS nfet_03v3 L=0.28u W=1.0u nf=1 ad=0.5p as=0.5p pd=3.0u ps=3.0u nrd=0 nrs=0 sa=0
+ sb=0 sd=0 m=1
Xp3 net5 clk VDD VDD pfet_03v3 L=0.28u W=2.0u nf=1 ad=1.0p as=1.0p pd=5.0u ps=5.0u nrd=0 nrs=0 sa=0
+ sb=0 sd=0 m=1
Xn2 net5 net4 net2 VSS nfet_03v3 L=0.28u W=1.0u nf=1 ad=0.5p as=0.5p pd=3.0u ps=3.0u nrd=0 nrs=0
+ sa=0 sb=0 sd=0 m=1
Xn3 net2 clk VSS VSS nfet_03v3 L=0.28u W=1.0u nf=1 ad=0.5p as=0.5p pd=3.0u ps=3.0u nrd=0 nrs=0 sa=0
+ sb=0 sd=0 m=1
Xp4 net6 net5 VDD VDD pfet_03v3 L=0.28u W=2.0u nf=1 ad=1.0p as=1.0p pd=5.0u ps=5.0u nrd=0 nrs=0 sa=0
+ sb=0 sd=0 m=1
Xn4 net6 clk net3 VSS nfet_03v3 L=0.28u W=1.0u nf=1 ad=0.5p as=0.5p pd=3.0u ps=3.0u nrd=0 nrs=0 sa=0
+ sb=0 sd=0 m=1
Xn5 net3 net5 VSS VSS nfet_03v3 L=0.28u W=1.0u nf=1 ad=0.5p as=0.5p pd=3.0u ps=3.0u nrd=0 nrs=0 sa=0
+ sb=0 sd=0 m=1
Xqp q net6 VDD VDD pfet_03v3 L=0.28u W=1.5u nf=1 ad=0.75p as=0.75p pd=4.0u ps=4.0u nrd=0 nrs=0 sa=0
+ sb=0 sd=0 m=1
Xqn q net6 VSS VSS nfet_03v3 L=0.28u W=0.6u nf=1 ad=0.3p as=0.3p pd=2.2u ps=2.2u nrd=0 nrs=0 sa=0
+ sb=0 sd=0 m=1
.ends

.end
